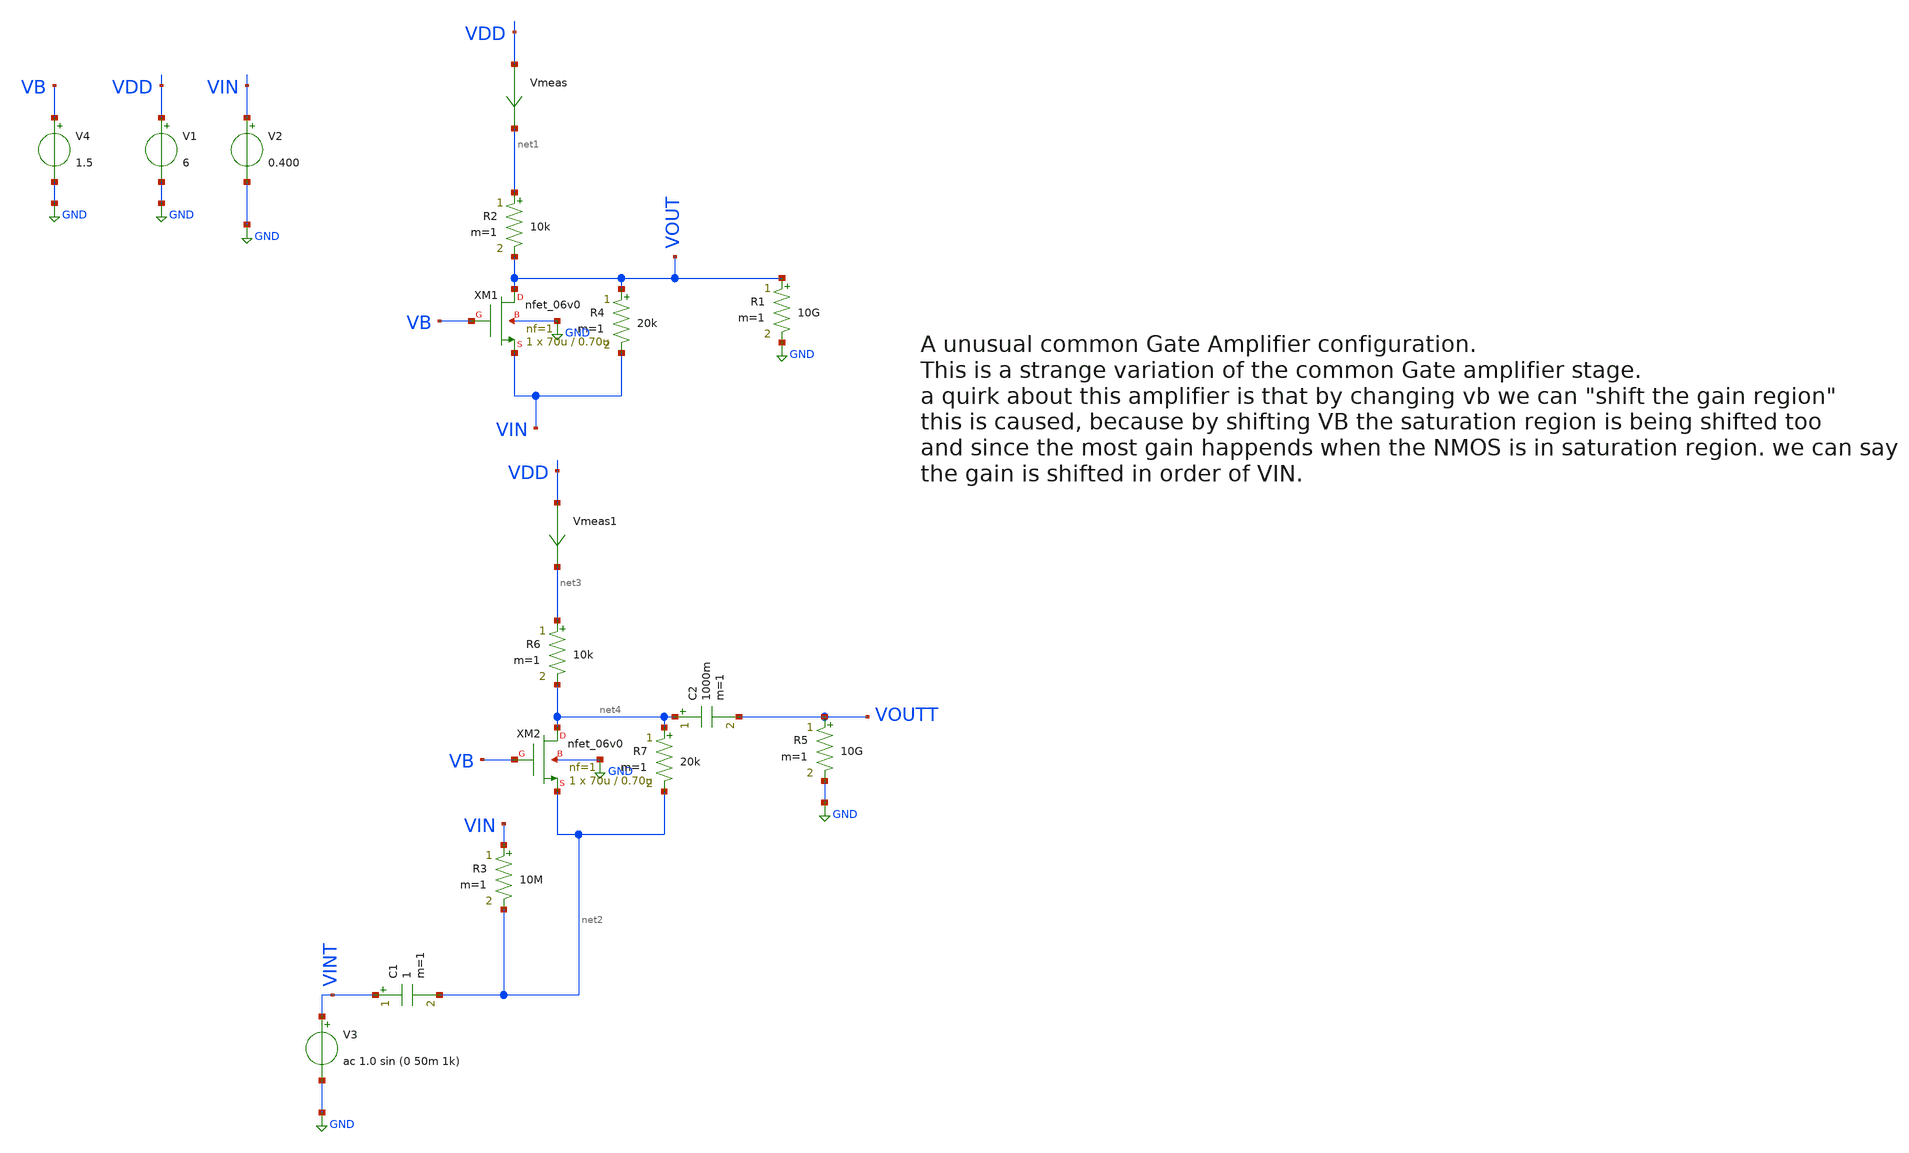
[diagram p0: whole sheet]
** sch_path: unusual_amplifiers/unusual_amp2.sch
**.subckt unusual_amp2
Vmeas VDD net1 0
.save i(vmeas)
V1 VDD GND 6
V2 VIN GND 0.400
V3 VINT GND ac 1.0 sin (0 50m 1k)
R3 VIN net2 10M m=1
R5 VOUTT GND 10G m=1
R1 VOUT GND 10G m=1
C1 VINT net2 1 m=1
XM1 VOUT VB VIN GND nfet_06v0 L=0.70u W=70u nf=1 ad='int((nf+1)/2) * W/nf * 0.18u' as='int((nf+2)/2) * W/nf * 0.18u'
+ pd='2*int((nf+1)/2) * (W/nf + 0.18u)' ps='2*int((nf+2)/2) * (W/nf + 0.18u)' nrd='0.18u / W' nrs='0.18u / W'
+ sa=0 sb=0 sd=0 m=1
R2 net1 VOUT 10k m=1
R4 VOUT VIN 20k m=1
Vmeas1 VDD net3 0
.save i(vmeas1)
XM2 net4 VB net2 GND nfet_06v0 L=0.70u W=70u nf=1 ad='int((nf+1)/2) * W/nf * 0.18u' as='int((nf+2)/2) * W/nf * 0.18u'
+ pd='2*int((nf+1)/2) * (W/nf + 0.18u)' ps='2*int((nf+2)/2) * (W/nf + 0.18u)' nrd='0.18u / W' nrs='0.18u / W'
+ sa=0 sb=0 sd=0 m=1
C2 net4 VOUTT 1000m m=1
V4 VB GND 1.5
R6 net3 net4 10k m=1
R7 net4 net2 20k m=1
**** begin user architecture code

**************************************************************
**************************************************************
**************************************************************
**************************************************************
**************************************************************
*LIBs*********************************************************
**************************************************************
**************************************************************
**************************************************************
**************************************************************
**************************************************************
.include $::180MCU_MODELS/design.ngspice
*.lib $::180MCU_MODELS/sm141064.ngspice statistical *use statistical if you want global and parameter mismatch
*.lib $::180MCU_MODELS/sm141064.ngspice res_statistical
.lib $::180MCU_MODELS/sm141064.ngspice typical
.lib $::180MCU_MODELS/sm141064.ngspice res_typical
.lib $::180MCU_MODELS/sm141064.ngspice moscap_typical
.lib $::180MCU_MODELS/sm141064.ngspice bjt_typical
.lib $::180MCU_MODELS/sm141064.ngspice diode_typical
.lib $::180MCU_MODELS/sm141064.ngspice mimcap_typical
**************************************************************
**************************************************************
**************************************************************
**************************************************************
**************************************************************
*Corners/montecarlo options***********************************
**************************************************************
**************************************************************
**************************************************************
**************************************************************
**************************************************************
.TEMP 27
.param   sw_stat_global = 1   sw_stat_mism = 1  mc_skew = 3  res_mc_skew = 3  cap_mc_skew = 3
+  fnoicor = 1
**************************************************************
**************************************************************
**************************************************************
**************************************************************
*SIMULATION and Plots*****************************************
**************************************************************
**************************************************************
**************************************************************
**************************************************************
.control
save all
dc V2 0 6 0.01
*dc simulation
plot v(VOUT) v(VIN) deriv(v(VOUT))
*ploting VIN VOUT and the voltage gain
plot i(Vmeas)
*ploting the current for curiosity
tran 100ns 2m
*transient simulation
plot (v(VINT)) (v(VOUTT))
*simple plot to exemplify the gain
fft v(VOUTT) v(VINT)
*fast fourier transfor
plot mag(v(VOUTT)) mag(v(VINT))
* analyse the frequency spectrum of the transient waves, to detect distortion
ac dec 20 1 50G
*simple ac simulation
plot v(VOUTT)
*gain in function of the input frequency
.endc

**** end user architecture code
**.ends
.GLOBAL GND
.end
